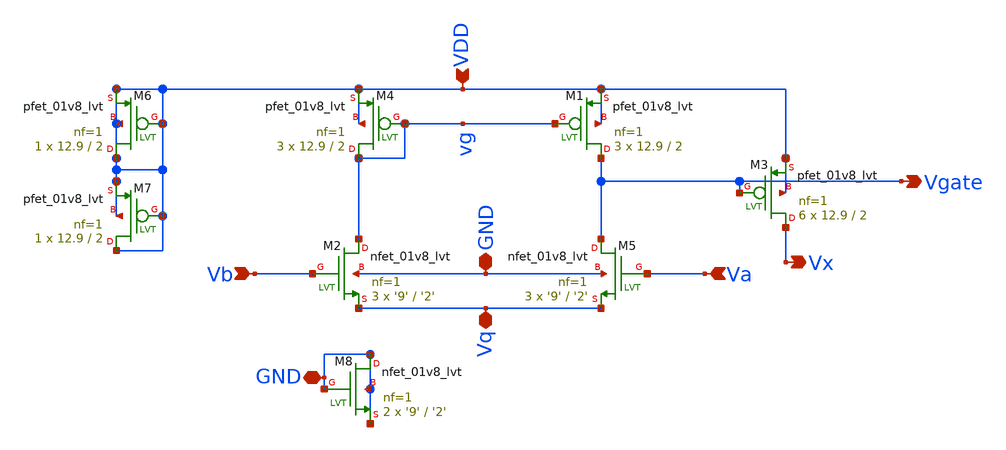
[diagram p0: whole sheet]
** sch_path: lvs/amplifier.sch
**.subckt amplifier VDD Vb Va Vq Vgate GND Vx GND
*.ipin VDD
*.ipin Vb
*.ipin Va
*.iopin Vq
*.opin Vgate
*.iopin GND
*.opin Vx
*.iopin GND
XM5 Vgate Va Vq GND sky130_fd_pr__nfet_01v8_lvt L='2' W='9' nf=1 ad='int((nf+1)/2) * W/nf * 0.29' as='int((nf+2)/2) * W/nf * 0.29'
+ pd='2*int((nf+1)/2) * (W/nf + 0.29)' ps='2*int((nf+2)/2) * (W/nf + 0.29)' nrd='0.29 / W' nrs='0.29 / W'
+ sa=0 sb=0 sd=0 mult=3 m=3
XM2 vg Vb Vq GND sky130_fd_pr__nfet_01v8_lvt L='2' W='9' nf=1 ad='int((nf+1)/2) * W/nf * 0.29' as='int((nf+2)/2) * W/nf * 0.29'
+ pd='2*int((nf+1)/2) * (W/nf + 0.29)' ps='2*int((nf+2)/2) * (W/nf + 0.29)' nrd='0.29 / W' nrs='0.29 / W'
+ sa=0 sb=0 sd=0 mult=3 m=3
XM4 vg vg VDD VDD sky130_fd_pr__pfet_01v8_lvt L=2 W=12.9 nf=1 ad='int((nf+1)/2) * W/nf * 0.29' as='int((nf+2)/2) * W/nf * 0.29'
+ pd='2*int((nf+1)/2) * (W/nf + 0.29)' ps='2*int((nf+2)/2) * (W/nf + 0.29)' nrd='0.29 / W' nrs='0.29 / W'
+ sa=0 sb=0 sd=0 mult=3 m=3
XM1 Vgate vg VDD VDD sky130_fd_pr__pfet_01v8_lvt L=2 W=12.9 nf=1 ad='int((nf+1)/2) * W/nf * 0.29' as='int((nf+2)/2) * W/nf * 0.29'
+ pd='2*int((nf+1)/2) * (W/nf + 0.29)' ps='2*int((nf+2)/2) * (W/nf + 0.29)' nrd='0.29 / W' nrs='0.29 / W'
+ sa=0 sb=0 sd=0 mult=3 m=3
XM3 Vx Vgate VDD VDD sky130_fd_pr__pfet_01v8_lvt L=2 W=12.9 nf=1 ad='int((nf+1)/2) * W/nf * 0.29' as='int((nf+2)/2) * W/nf * 0.29'
+ pd='2*int((nf+1)/2) * (W/nf + 0.29)' ps='2*int((nf+2)/2) * (W/nf + 0.29)' nrd='0.29 / W' nrs='0.29 / W'
+ sa=0 sb=0 sd=0 mult=6 m=6
XM6 VDD VDD VDD VDD sky130_fd_pr__pfet_01v8_lvt L=2 W=12.9 nf=1 ad='int((nf+1)/2) * W/nf * 0.29' as='int((nf+2)/2) * W/nf * 0.29'
+ pd='2*int((nf+1)/2) * (W/nf + 0.29)' ps='2*int((nf+2)/2) * (W/nf + 0.29)' nrd='0.29 / W' nrs='0.29 / W'
+ sa=0 sb=0 sd=0 mult=1 m=1
XM7 VDD VDD VDD VDD sky130_fd_pr__pfet_01v8_lvt L=2 W=12.9 nf=1 ad='int((nf+1)/2) * W/nf * 0.29' as='int((nf+2)/2) * W/nf * 0.29'
+ pd='2*int((nf+1)/2) * (W/nf + 0.29)' ps='2*int((nf+2)/2) * (W/nf + 0.29)' nrd='0.29 / W' nrs='0.29 / W'
+ sa=0 sb=0 sd=0 mult=1 m=1
XM8 GND GND GND GND sky130_fd_pr__nfet_01v8_lvt L='2' W='9' nf=1 ad='int((nf+1)/2) * W/nf * 0.29' as='int((nf+2)/2) * W/nf * 0.29'
+ pd='2*int((nf+1)/2) * (W/nf + 0.29)' ps='2*int((nf+2)/2) * (W/nf + 0.29)' nrd='0.29 / W' nrs='0.29 / W'
+ sa=0 sb=0 sd=0 mult=2 m=2
**.ends
.end
